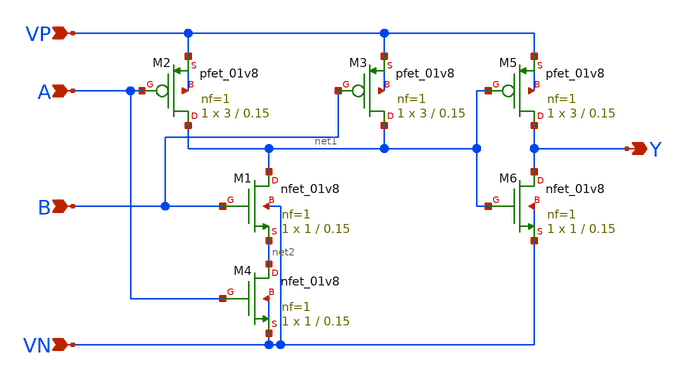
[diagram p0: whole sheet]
** sch_path: APIC-UTS/schematic/goldwin_and/goldwin_and.sch
**.subckt goldwin_and A B Y VP VN
*.ipin A
*.ipin B
*.opin Y
*.ipin VP
*.ipin VN
XM1 net1 B net2 VN sky130_fd_pr__nfet_01v8 L=0.15 W=1 nf=1 ad='int((nf+1)/2) * W/nf * 0.29' as='int((nf+2)/2) * W/nf * 0.29'
+ pd='2*int((nf+1)/2) * (W/nf + 0.29)' ps='2*int((nf+2)/2) * (W/nf + 0.29)' nrd='0.29 / W' nrs='0.29 / W'
+ sa=0 sb=0 sd=0 mult=1 m=1
XM4 net2 A VN VN sky130_fd_pr__nfet_01v8 L=0.15 W=1 nf=1 ad='int((nf+1)/2) * W/nf * 0.29' as='int((nf+2)/2) * W/nf * 0.29'
+ pd='2*int((nf+1)/2) * (W/nf + 0.29)' ps='2*int((nf+2)/2) * (W/nf + 0.29)' nrd='0.29 / W' nrs='0.29 / W'
+ sa=0 sb=0 sd=0 mult=1 m=1
XM6 Y net1 VN VN sky130_fd_pr__nfet_01v8 L=0.15 W=1 nf=1 ad='int((nf+1)/2) * W/nf * 0.29' as='int((nf+2)/2) * W/nf * 0.29'
+ pd='2*int((nf+1)/2) * (W/nf + 0.29)' ps='2*int((nf+2)/2) * (W/nf + 0.29)' nrd='0.29 / W' nrs='0.29 / W'
+ sa=0 sb=0 sd=0 mult=1 m=1
XM2 net1 A VP VP sky130_fd_pr__pfet_01v8 L=0.15 W=3 nf=1 ad='int((nf+1)/2) * W/nf * 0.29' as='int((nf+2)/2) * W/nf * 0.29'
+ pd='2*int((nf+1)/2) * (W/nf + 0.29)' ps='2*int((nf+2)/2) * (W/nf + 0.29)' nrd='0.29 / W' nrs='0.29 / W'
+ sa=0 sb=0 sd=0 mult=1 m=1
XM3 net1 B VP VP sky130_fd_pr__pfet_01v8 L=0.15 W=3 nf=1 ad='int((nf+1)/2) * W/nf * 0.29' as='int((nf+2)/2) * W/nf * 0.29'
+ pd='2*int((nf+1)/2) * (W/nf + 0.29)' ps='2*int((nf+2)/2) * (W/nf + 0.29)' nrd='0.29 / W' nrs='0.29 / W'
+ sa=0 sb=0 sd=0 mult=1 m=1
XM5 Y net1 VP VP sky130_fd_pr__pfet_01v8 L=0.15 W=3 nf=1 ad='int((nf+1)/2) * W/nf * 0.29' as='int((nf+2)/2) * W/nf * 0.29'
+ pd='2*int((nf+1)/2) * (W/nf + 0.29)' ps='2*int((nf+2)/2) * (W/nf + 0.29)' nrd='0.29 / W' nrs='0.29 / W'
+ sa=0 sb=0 sd=0 mult=1 m=1
**.ends
.end
